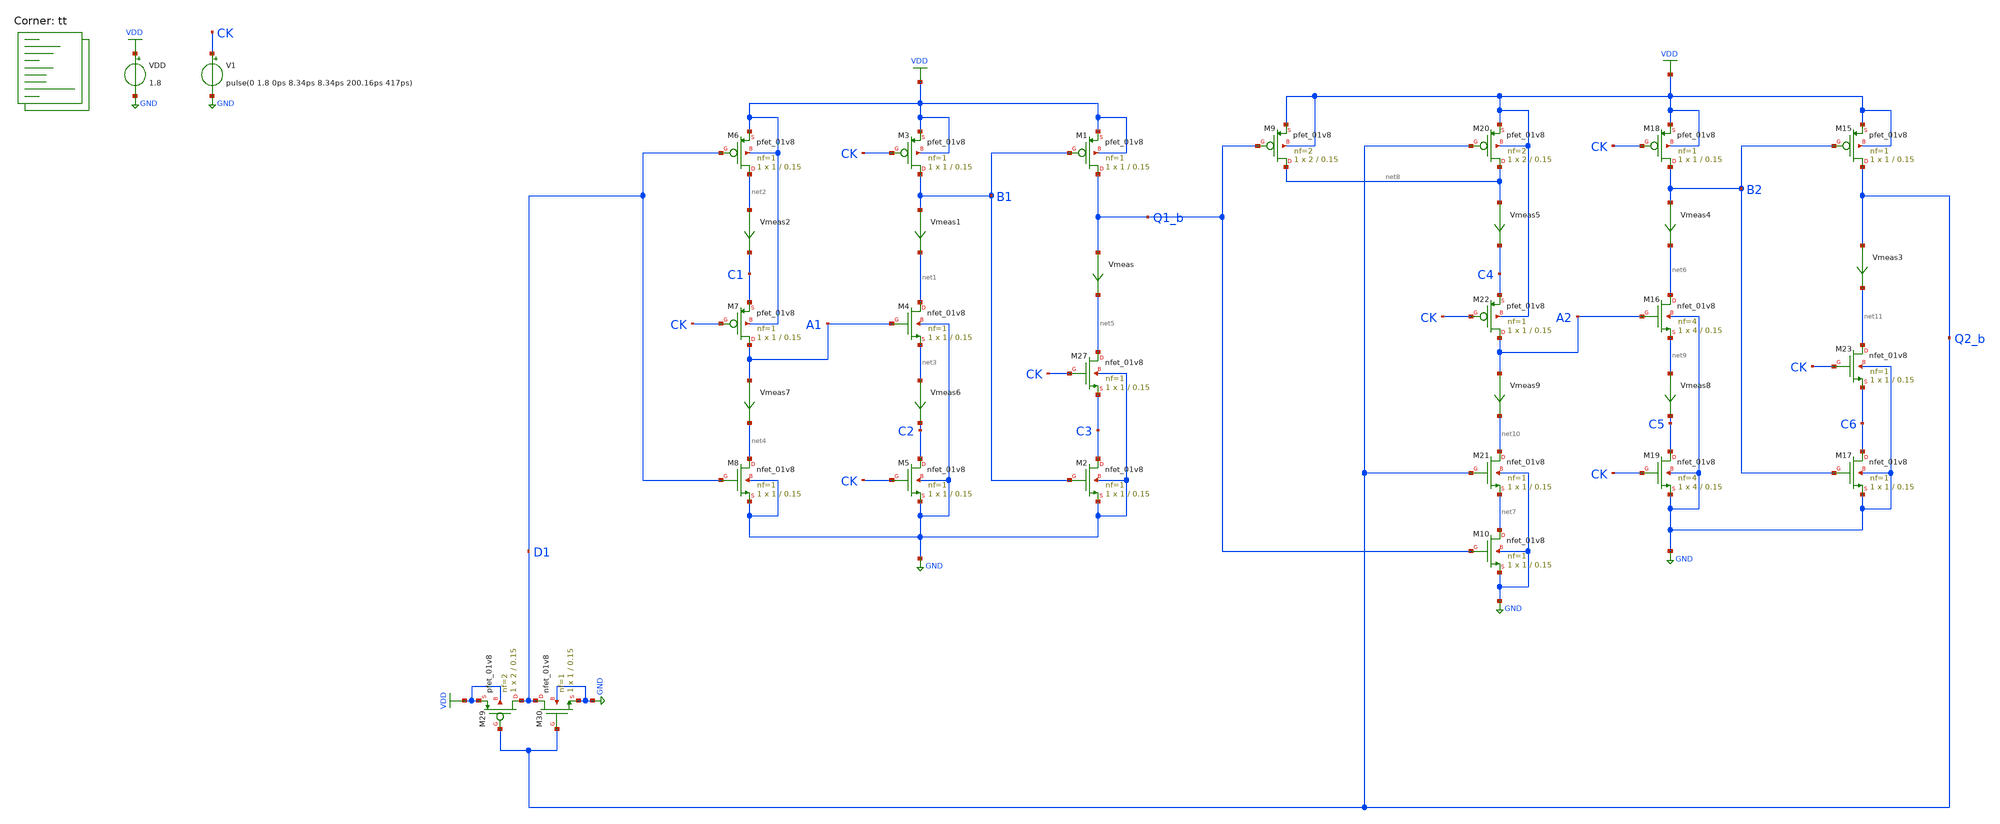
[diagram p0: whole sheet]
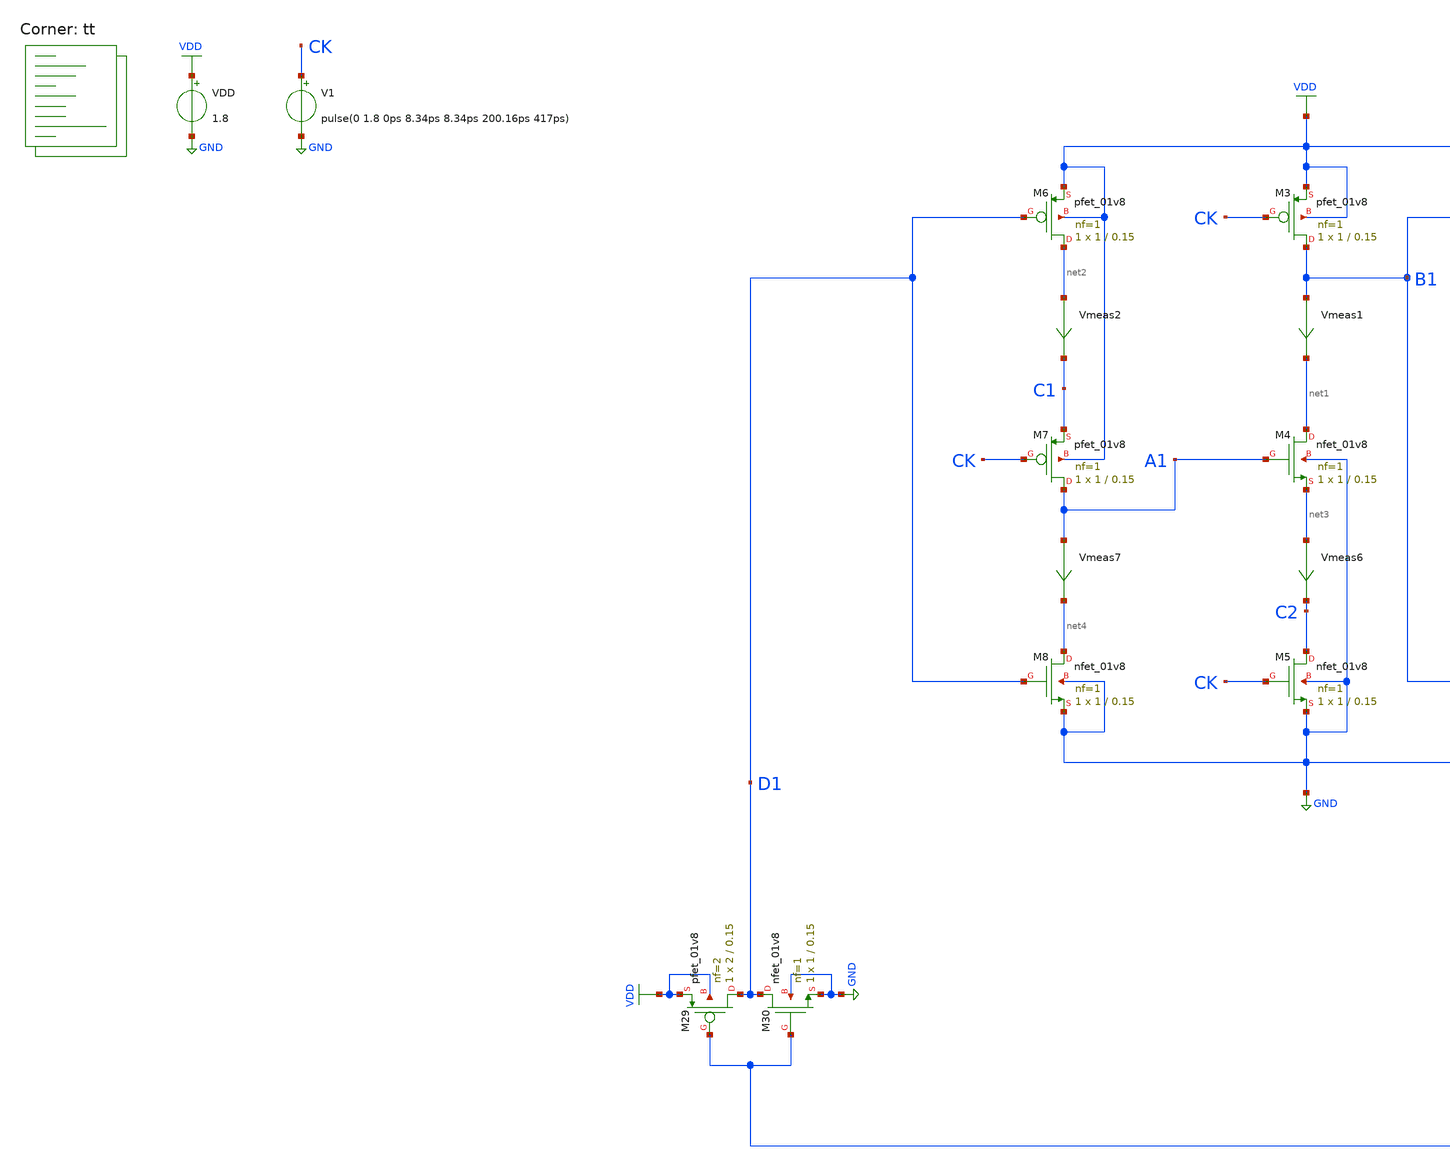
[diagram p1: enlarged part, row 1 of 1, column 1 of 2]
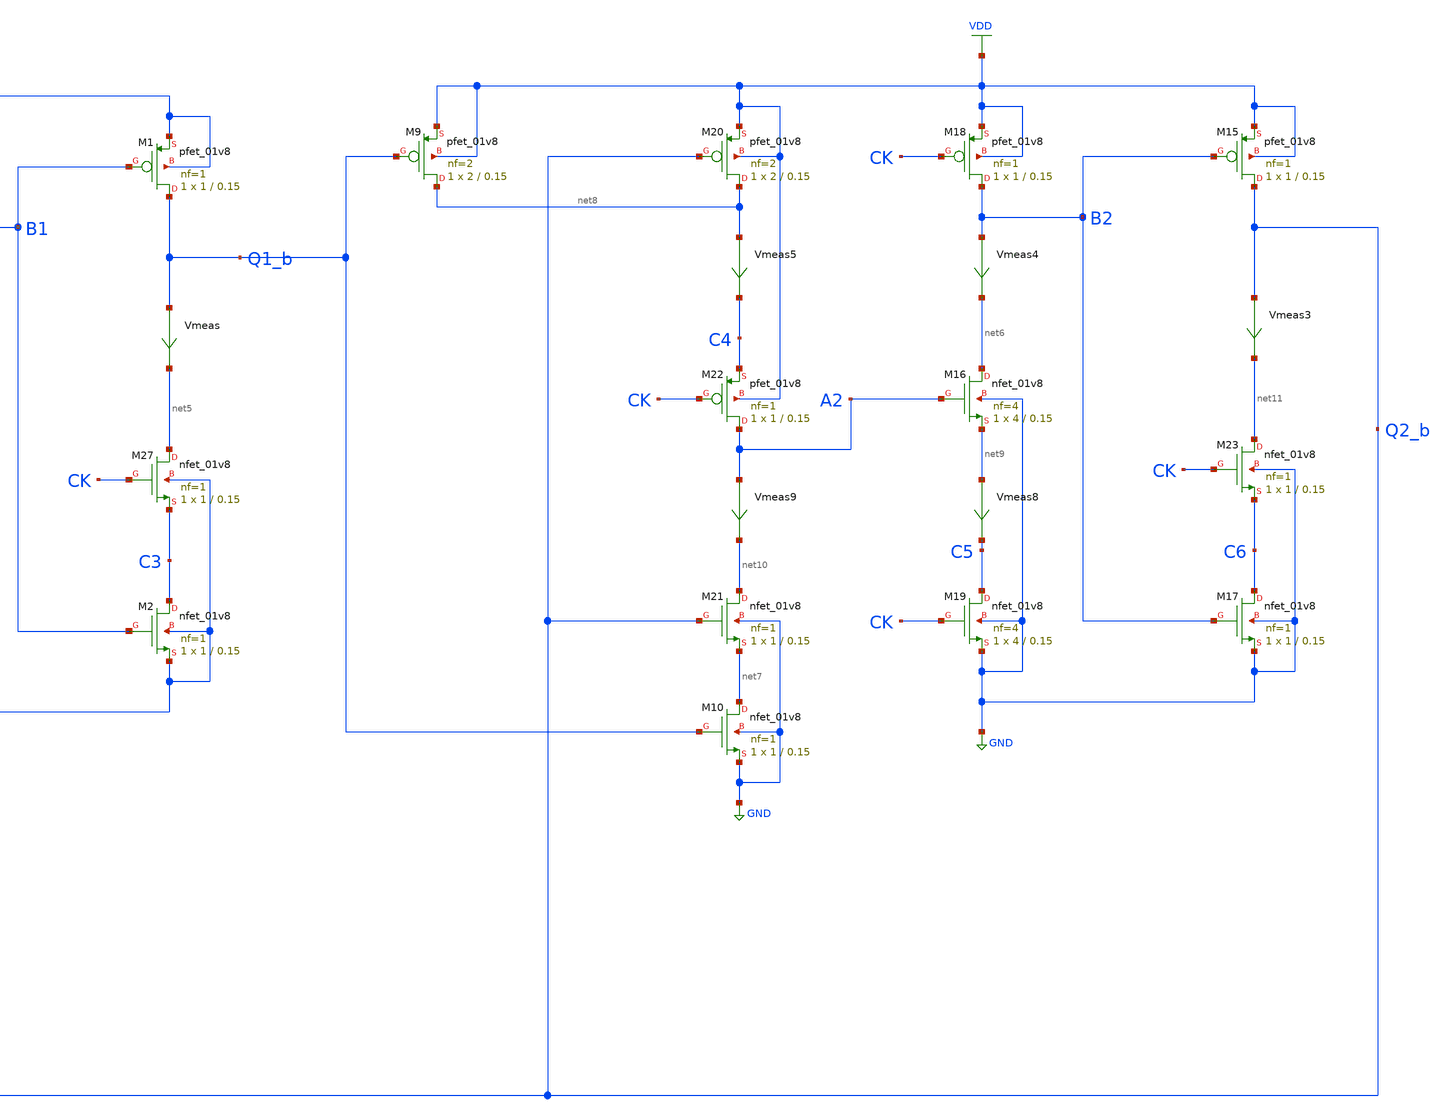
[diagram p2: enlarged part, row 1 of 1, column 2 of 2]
** sch_path: projects/pll/divider/xschem_ngspice/tb_TSPC_FF_divide3_3.sch
**.subckt tb_TSPC_FF_divide3_3
VDD VDD GND 1.8
XM1 Q1_b B1 VDD VDD sky130_fd_pr__pfet_01v8 L=0.15 W=1 nf=1 ad='int((nf+1)/2) * W/nf * 0.29' as='int((nf+2)/2) * W/nf * 0.29'
+ pd='2*int((nf+1)/2) * (W/nf + 0.29)' ps='2*int((nf+2)/2) * (W/nf + 0.29)' nrd='0.29 / W' nrs='0.29 / W'
+ sa=0 sb=0 sd=0 mult=1 m=1
XM4 net1 A1 net3 GND sky130_fd_pr__nfet_01v8 L=0.15 W=1 nf=1 ad='int((nf+1)/2) * W/nf * 0.29' as='int((nf+2)/2) * W/nf * 0.29'
+ pd='2*int((nf+1)/2) * (W/nf + 0.29)' ps='2*int((nf+2)/2) * (W/nf + 0.29)' nrd='0.29 / W' nrs='0.29 / W'
+ sa=0 sb=0 sd=0 mult=1 m=1
Vmeas Q1_b net5 0
.save i(vmeas)
XM2 C3 B1 GND GND sky130_fd_pr__nfet_01v8 L=0.15 W=1 nf=1 ad='int((nf+1)/2) * W/nf * 0.29' as='int((nf+2)/2) * W/nf * 0.29'
+ pd='2*int((nf+1)/2) * (W/nf + 0.29)' ps='2*int((nf+2)/2) * (W/nf + 0.29)' nrd='0.29 / W' nrs='0.29 / W'
+ sa=0 sb=0 sd=0 mult=1 m=1
XM3 B1 CK VDD VDD sky130_fd_pr__pfet_01v8 L=0.15 W=1 nf=1 ad='int((nf+1)/2) * W/nf * 0.29' as='int((nf+2)/2) * W/nf * 0.29'
+ pd='2*int((nf+1)/2) * (W/nf + 0.29)' ps='2*int((nf+2)/2) * (W/nf + 0.29)' nrd='0.29 / W' nrs='0.29 / W'
+ sa=0 sb=0 sd=0 mult=1 m=1
XM5 C2 CK GND GND sky130_fd_pr__nfet_01v8 L=0.15 W=1 nf=1 ad='int((nf+1)/2) * W/nf * 0.29' as='int((nf+2)/2) * W/nf * 0.29'
+ pd='2*int((nf+1)/2) * (W/nf + 0.29)' ps='2*int((nf+2)/2) * (W/nf + 0.29)' nrd='0.29 / W' nrs='0.29 / W'
+ sa=0 sb=0 sd=0 mult=1 m=1
Vmeas1 B1 net1 0
.save i(vmeas1)
XM6 net2 D1 VDD VDD sky130_fd_pr__pfet_01v8 L=0.15 W=1 nf=1 ad='int((nf+1)/2) * W/nf * 0.29' as='int((nf+2)/2) * W/nf * 0.29'
+ pd='2*int((nf+1)/2) * (W/nf + 0.29)' ps='2*int((nf+2)/2) * (W/nf + 0.29)' nrd='0.29 / W' nrs='0.29 / W'
+ sa=0 sb=0 sd=0 mult=1 m=1
XM8 net4 D1 GND GND sky130_fd_pr__nfet_01v8 L=0.15 W=1 nf=1 ad='int((nf+1)/2) * W/nf * 0.29' as='int((nf+2)/2) * W/nf * 0.29'
+ pd='2*int((nf+1)/2) * (W/nf + 0.29)' ps='2*int((nf+2)/2) * (W/nf + 0.29)' nrd='0.29 / W' nrs='0.29 / W'
+ sa=0 sb=0 sd=0 mult=1 m=1
Vmeas2 net2 C1 0
.save i(vmeas2)
XM7 A1 CK C1 VDD sky130_fd_pr__pfet_01v8 L=0.15 W=1 nf=1 ad='int((nf+1)/2) * W/nf * 0.29' as='int((nf+2)/2) * W/nf * 0.29'
+ pd='2*int((nf+1)/2) * (W/nf + 0.29)' ps='2*int((nf+2)/2) * (W/nf + 0.29)' nrd='0.29 / W' nrs='0.29 / W'
+ sa=0 sb=0 sd=0 mult=1 m=1
Vmeas6 net3 C2 0
.save i(vmeas6)
Vmeas7 A1 net4 0
.save i(vmeas7)
XM27 net5 CK C3 GND sky130_fd_pr__nfet_01v8 L=0.15 W=1 nf=1 ad='int((nf+1)/2) * W/nf * 0.29' as='int((nf+2)/2) * W/nf * 0.29'
+ pd='2*int((nf+1)/2) * (W/nf + 0.29)' ps='2*int((nf+2)/2) * (W/nf + 0.29)' nrd='0.29 / W' nrs='0.29 / W'
+ sa=0 sb=0 sd=0 mult=1 m=1
XM15 Q2_b B2 VDD VDD sky130_fd_pr__pfet_01v8 L=0.15 W=1 nf=1 ad='int((nf+1)/2) * W/nf * 0.29' as='int((nf+2)/2) * W/nf * 0.29'
+ pd='2*int((nf+1)/2) * (W/nf + 0.29)' ps='2*int((nf+2)/2) * (W/nf + 0.29)' nrd='0.29 / W' nrs='0.29 / W'
+ sa=0 sb=0 sd=0 mult=1 m=1
XM16 net6 A2 net9 GND sky130_fd_pr__nfet_01v8 L=0.15 W=4 nf=4 ad='int((nf+1)/2) * W/nf * 0.29' as='int((nf+2)/2) * W/nf * 0.29'
+ pd='2*int((nf+1)/2) * (W/nf + 0.29)' ps='2*int((nf+2)/2) * (W/nf + 0.29)' nrd='0.29 / W' nrs='0.29 / W'
+ sa=0 sb=0 sd=0 mult=1 m=1
Vmeas3 Q2_b net11 0
.save i(vmeas3)
XM17 C6 B2 GND GND sky130_fd_pr__nfet_01v8 L=0.15 W=1 nf=1 ad='int((nf+1)/2) * W/nf * 0.29' as='int((nf+2)/2) * W/nf * 0.29'
+ pd='2*int((nf+1)/2) * (W/nf + 0.29)' ps='2*int((nf+2)/2) * (W/nf + 0.29)' nrd='0.29 / W' nrs='0.29 / W'
+ sa=0 sb=0 sd=0 mult=1 m=1
XM18 B2 CK VDD VDD sky130_fd_pr__pfet_01v8 L=0.15 W=1 nf=1 ad='int((nf+1)/2) * W/nf * 0.29' as='int((nf+2)/2) * W/nf * 0.29'
+ pd='2*int((nf+1)/2) * (W/nf + 0.29)' ps='2*int((nf+2)/2) * (W/nf + 0.29)' nrd='0.29 / W' nrs='0.29 / W'
+ sa=0 sb=0 sd=0 mult=1 m=1
XM19 C5 CK GND GND sky130_fd_pr__nfet_01v8 L=0.15 W=4 nf=4 ad='int((nf+1)/2) * W/nf * 0.29' as='int((nf+2)/2) * W/nf * 0.29'
+ pd='2*int((nf+1)/2) * (W/nf + 0.29)' ps='2*int((nf+2)/2) * (W/nf + 0.29)' nrd='0.29 / W' nrs='0.29 / W'
+ sa=0 sb=0 sd=0 mult=1 m=1
Vmeas4 B2 net6 0
.save i(vmeas4)
XM20 net8 Q2_b VDD VDD sky130_fd_pr__pfet_01v8 L=0.15 W=2 nf=2 ad='int((nf+1)/2) * W/nf * 0.29' as='int((nf+2)/2) * W/nf * 0.29'
+ pd='2*int((nf+1)/2) * (W/nf + 0.29)' ps='2*int((nf+2)/2) * (W/nf + 0.29)' nrd='0.29 / W' nrs='0.29 / W'
+ sa=0 sb=0 sd=0 mult=1 m=1
XM21 net10 Q2_b net7 GND sky130_fd_pr__nfet_01v8 L=0.15 W=1 nf=1 ad='int((nf+1)/2) * W/nf * 0.29' as='int((nf+2)/2) * W/nf * 0.29'
+ pd='2*int((nf+1)/2) * (W/nf + 0.29)' ps='2*int((nf+2)/2) * (W/nf + 0.29)' nrd='0.29 / W' nrs='0.29 / W'
+ sa=0 sb=0 sd=0 mult=1 m=1
Vmeas5 net8 C4 0
.save i(vmeas5)
XM22 A2 CK C4 VDD sky130_fd_pr__pfet_01v8 L=0.15 W=1 nf=1 ad='int((nf+1)/2) * W/nf * 0.29' as='int((nf+2)/2) * W/nf * 0.29'
+ pd='2*int((nf+1)/2) * (W/nf + 0.29)' ps='2*int((nf+2)/2) * (W/nf + 0.29)' nrd='0.29 / W' nrs='0.29 / W'
+ sa=0 sb=0 sd=0 mult=1 m=1
Vmeas8 net9 C5 0
.save i(vmeas8)
Vmeas9 A2 net10 0
.save i(vmeas9)
XM23 net11 CK C6 GND sky130_fd_pr__nfet_01v8 L=0.15 W=1 nf=1 ad='int((nf+1)/2) * W/nf * 0.29' as='int((nf+2)/2) * W/nf * 0.29'
+ pd='2*int((nf+1)/2) * (W/nf + 0.29)' ps='2*int((nf+2)/2) * (W/nf + 0.29)' nrd='0.29 / W' nrs='0.29 / W'
+ sa=0 sb=0 sd=0 mult=1 m=1
V1 CK GND pulse(0 1.8 0ps 8.34ps 8.34ps 200.16ps 417ps)
XM29 D1 Q2_b VDD VDD sky130_fd_pr__pfet_01v8 L=0.15 W=2 nf=2 ad='int((nf+1)/2) * W/nf * 0.29' as='int((nf+2)/2) * W/nf * 0.29'
+ pd='2*int((nf+1)/2) * (W/nf + 0.29)' ps='2*int((nf+2)/2) * (W/nf + 0.29)' nrd='0.29 / W' nrs='0.29 / W'
+ sa=0 sb=0 sd=0 mult=1 m=1
XM30 D1 Q2_b GND GND sky130_fd_pr__nfet_01v8 L=0.15 W=1 nf=1 ad='int((nf+1)/2) * W/nf * 0.29' as='int((nf+2)/2) * W/nf * 0.29'
+ pd='2*int((nf+1)/2) * (W/nf + 0.29)' ps='2*int((nf+2)/2) * (W/nf + 0.29)' nrd='0.29 / W' nrs='0.29 / W'
+ sa=0 sb=0 sd=0 mult=1 m=1
XM9 net8 Q1_b VDD VDD sky130_fd_pr__pfet_01v8 L=0.15 W=2 nf=2 ad='int((nf+1)/2) * W/nf * 0.29' as='int((nf+2)/2) * W/nf * 0.29'
+ pd='2*int((nf+1)/2) * (W/nf + 0.29)' ps='2*int((nf+2)/2) * (W/nf + 0.29)' nrd='0.29 / W' nrs='0.29 / W'
+ sa=0 sb=0 sd=0 mult=1 m=1
XM10 net7 Q1_b GND GND sky130_fd_pr__nfet_01v8 L=0.15 W=1 nf=1 ad='int((nf+1)/2) * W/nf * 0.29' as='int((nf+2)/2) * W/nf * 0.29'
+ pd='2*int((nf+1)/2) * (W/nf + 0.29)' ps='2*int((nf+2)/2) * (W/nf + 0.29)' nrd='0.29 / W' nrs='0.29 / W'
+ sa=0 sb=0 sd=0 mult=1 m=1
**** begin user architecture code



.include /foss/pdks/sky130A/libs.ref/sky130_fd_sc_hd/spice/sky130_fd_sc_hd.spice


.save @m.xm1.msky130_fd_pr__pfet_01v8[gm] @m.xm27.msky130_fd_pr__nfet_01v8[gm] @m.xm2.msky130_fd_pr__nfet_01v8[gm] @m.xm3.msky130_fd_pr__pfet_01v8[gm] @m.xm4.msky130_fd_pr__nfet_01v8[gm] @m.xm5.msky130_fd_pr__nfet_01v8[gm] @m.xm6.msky130_fd_pr__pfet_01v8[gm] @m.xm7.msky130_fd_pr__pfet_01v8[gm] @m.xm8.msky130_fd_pr__nfet_01v8[gm]

.option method=gear
.option wnflag=1
.option savecurrents


*.ic v(d)=0
.ic v(q1_b)=1.8
.ic v(q2_b)=1.8

.control

  save v(d1) v(d2) v(q1) v(q2) v(q1_b) v(q2_b) v(q3) v(q4) v(q3_b) v(q4_b) v(a1) v(a2) v(a3) v(a4)
+ v(b1) v(b2) v(b3) v(b4) v(c1) v(c2) v(c3) v(c4) v(c5) v(c6) v(c7) v(c8) v(ck) v(ck1) v(ck1_b)
  * save all
  * tran 0.1n 1u
  tran 1p 20n

  remzerovec
  write tb_TSPC_FF_divide3_3.raw
  * set appendwrite

.endc



.lib $::SKYWATER_MODELS/sky130.lib.spice tt
**** end user architecture code
**.ends
.GLOBAL GND
.GLOBAL VDD
.end
